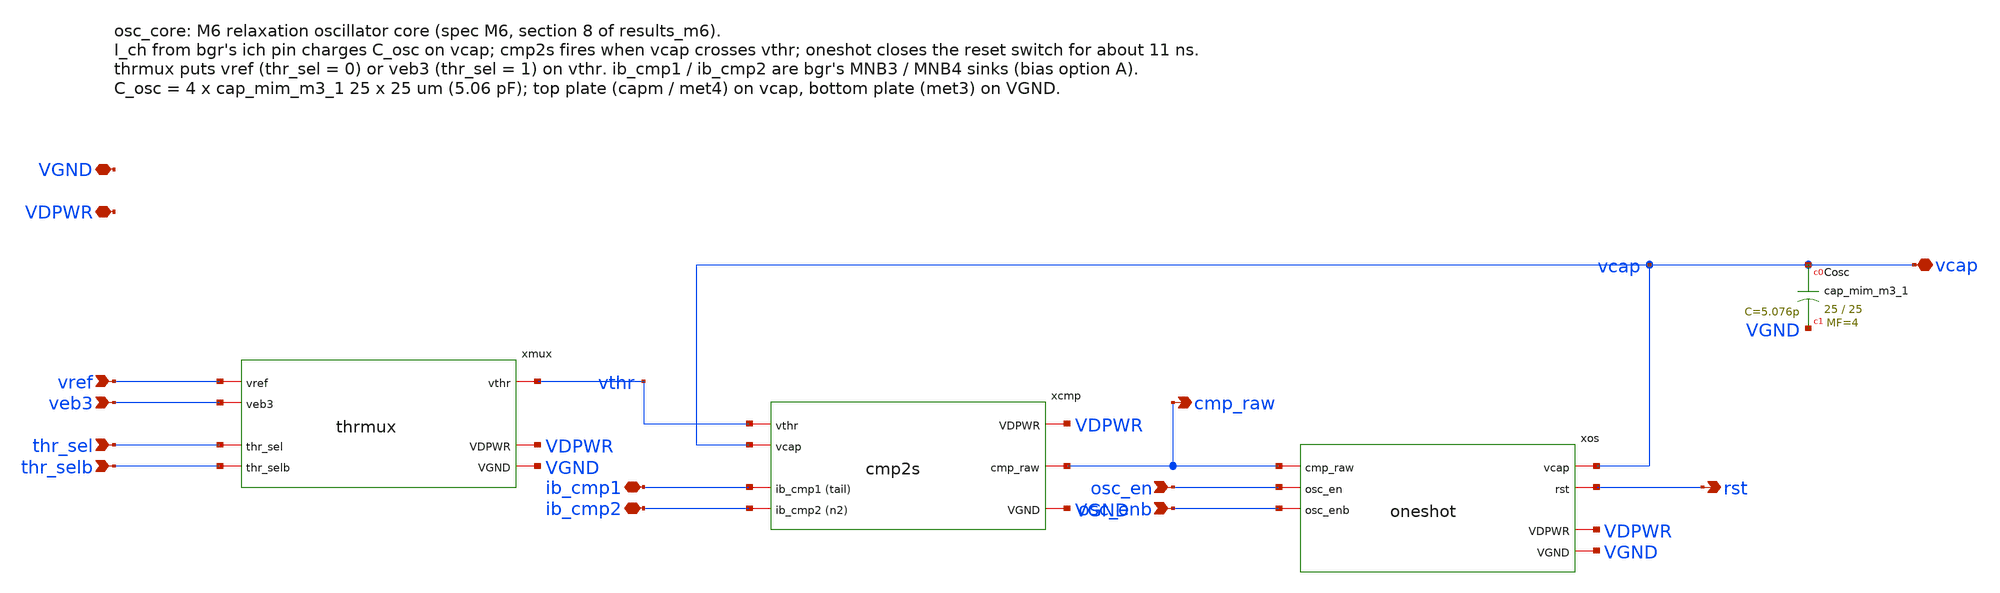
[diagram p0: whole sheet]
** sch_path: xschem/osc_core.sch
**.subckt osc_core vref veb3 thr_sel thr_selb ib_cmp1 ib_cmp2 cmp_raw osc_en osc_enb vcap rst VDPWR
*+ VGND
*.ipin vref
*.ipin veb3
*.ipin thr_sel
*.ipin thr_selb
*.iopin ib_cmp1
*.iopin ib_cmp2
*.opin cmp_raw
*.ipin osc_en
*.ipin osc_enb
*.iopin vcap
*.opin rst
*.iopin VDPWR
*.iopin VGND
xmux vref veb3 thr_sel thr_selb vthr VDPWR VGND thrmux
xcmp vthr vcap ib_cmp1 ib_cmp2 VDPWR cmp_raw VGND cmp2s
xos cmp_raw osc_en osc_enb vcap rst VDPWR VGND oneshot
XCosc vcap VGND sky130_fd_pr__cap_mim_m3_1 W=25 L=25 MF=4 m=4
**.ends

* expanding   symbol:  thrmux.sym # of pins=7
** sym_path: xschem/thrmux.sym
** sch_path: xschem/thrmux.sch
.subckt thrmux vref veb3 thr_sel thr_selb vthr VDPWR VGND
*.ipin thr_sel
*.ipin thr_selb
*.ipin vref
*.ipin veb3
*.iopin vthr
*.iopin VDPWR
*.iopin VGND
xn1 thr_sel seb VGND VGND VDPWR VDPWR sref sky130_fd_sc_hd__nor2_1
xn2 sref thr_selb VGND VGND VDPWR VDPWR seb sky130_fd_sc_hd__nor2_1
xi1 sref VGND VGND VDPWR VDPWR srefb sky130_fd_sc_hd__inv_1
xi2 seb VGND VGND VDPWR VDPWR sebb sky130_fd_sc_hd__inv_1
XMTN1 vref sref vthr VGND sky130_fd_pr__nfet_01v8_lvt L=0.5 W=2 nf=1 ad='int((1 + 1)/2) * 2 / 1 * 0.29'
+ as='int((1 + 2)/2) * 2 / 1 * 0.29' pd='2*int((1 + 1)/2) * (2 / 1 + 0.29)' ps='2*int((1 + 2)/2) * (2 / 1 + 0.29)'
+ nrd='0.29 / 2 ' nrs='0.29 / 2 ' sa=0 sb=0 sd=0 mult=1 m=1
XMTP1 vthr srefb vref VDPWR sky130_fd_pr__pfet_01v8_lvt L=0.5 W=4 nf=1 ad='int((1 + 1)/2) * 4 / 1 * 0.29'
+ as='int((1 + 2)/2) * 4 / 1 * 0.29' pd='2*int((1 + 1)/2) * (4 / 1 + 0.29)' ps='2*int((1 + 2)/2) * (4 / 1 + 0.29)'
+ nrd='0.29 / 4 ' nrs='0.29 / 4 ' sa=0 sb=0 sd=0 mult=1 m=1
XMTN2 vthr seb veb3 VGND sky130_fd_pr__nfet_01v8_lvt L=0.5 W=2 nf=1 ad='int((1 + 1)/2) * 2 / 1 * 0.29'
+ as='int((1 + 2)/2) * 2 / 1 * 0.29' pd='2*int((1 + 1)/2) * (2 / 1 + 0.29)' ps='2*int((1 + 2)/2) * (2 / 1 + 0.29)'
+ nrd='0.29 / 2 ' nrs='0.29 / 2 ' sa=0 sb=0 sd=0 mult=1 m=1
XMTP2 veb3 sebb vthr VDPWR sky130_fd_pr__pfet_01v8_lvt L=0.5 W=4 nf=1 ad='int((1 + 1)/2) * 4 / 1 * 0.29'
+ as='int((1 + 2)/2) * 4 / 1 * 0.29' pd='2*int((1 + 1)/2) * (4 / 1 + 0.29)' ps='2*int((1 + 2)/2) * (4 / 1 + 0.29)'
+ nrd='0.29 / 4 ' nrs='0.29 / 4 ' sa=0 sb=0 sd=0 mult=1 m=1
.ends


* expanding   symbol:  cmp2s.sym # of pins=7
** sym_path: xschem/cmp2s.sym
** sch_path: xschem/cmp2s.sch
.subckt cmp2s vthr vcap ib_cmp1 ib_cmp2 VDPWR cmp_raw VGND
*.iopin VDPWR
*.iopin VGND
*.ipin vthr
*.ipin vcap
*.iopin ib_cmp1
*.iopin ib_cmp2
*.opin cmp_raw
XM2a nd nd VDPWR VDPWR sky130_fd_pr__pfet_01v8_lvt L=4 W=4 nf=1 ad='int((1 + 1)/2) * 4 / 1 * 0.29' as='int((1 + 2)/2) * 4 / 1 * 0.29'
+ pd='2*int((1 + 1)/2) * (4 / 1 + 0.29)' ps='2*int((1 + 2)/2) * (4 / 1 + 0.29)' nrd='0.29 / 4 ' nrs='0.29 / 4 '
+ sa=0 sb=0 sd=0 mult=8 m=8
XM2b n1 nd VDPWR VDPWR sky130_fd_pr__pfet_01v8_lvt L=4 W=4 nf=1 ad='int((1 + 1)/2) * 4 / 1 * 0.29' as='int((1 + 2)/2) * 4 / 1 * 0.29'
+ pd='2*int((1 + 1)/2) * (4 / 1 + 0.29)' ps='2*int((1 + 2)/2) * (4 / 1 + 0.29)' nrd='0.29 / 4 ' nrs='0.29 / 4 '
+ sa=0 sb=0 sd=0 mult=8 m=8
XM1a nd vthr ib_cmp1 VGND sky130_fd_pr__nfet_01v8_lvt L=1.75 W=10 nf=1 ad='int((1 + 1)/2) * 10 / 1 * 0.29'
+ as='int((1 + 2)/2) * 10 / 1 * 0.29' pd='2*int((1 + 1)/2) * (10 / 1 + 0.29)' ps='2*int((1 + 2)/2) * (10 / 1 + 0.29)'
+ nrd='0.29 / 10 ' nrs='0.29 / 10 ' sa=0 sb=0 sd=0 mult=6 m=6
XM1b n1 vcap ib_cmp1 VGND sky130_fd_pr__nfet_01v8_lvt L=1.75 W=10 nf=1 ad='int((1 + 1)/2) * 10 / 1 * 0.29'
+ as='int((1 + 2)/2) * 10 / 1 * 0.29' pd='2*int((1 + 1)/2) * (10 / 1 + 0.29)' ps='2*int((1 + 2)/2) * (10 / 1 + 0.29)'
+ nrd='0.29 / 10 ' nrs='0.29 / 10 ' sa=0 sb=0 sd=0 mult=6 m=6
XM3 ib_cmp2 n1 VDPWR VDPWR sky130_fd_pr__pfet_01v8_lvt L=1 W=4 nf=1 ad='int((1 + 1)/2) * 4 / 1 * 0.29'
+ as='int((1 + 2)/2) * 4 / 1 * 0.29' pd='2*int((1 + 1)/2) * (4 / 1 + 0.29)' ps='2*int((1 + 2)/2) * (4 / 1 + 0.29)'
+ nrd='0.29 / 4 ' nrs='0.29 / 4 ' sa=0 sb=0 sd=0 mult=3 m=3
XMIP x ib_cmp2 VDPWR VDPWR sky130_fd_pr__pfet_01v8 L=1 W=0.42 nf=1 ad='int((1 + 1)/2) * 0.42 / 1 * 0.29'
+ as='int((1 + 2)/2) * 0.42 / 1 * 0.29' pd='2*int((1 + 1)/2) * (0.42 / 1 + 0.29)' ps='2*int((1 + 2)/2) * (0.42 / 1 + 0.29)'
+ nrd='0.29 / 0.42 ' nrs='0.29 / 0.42 ' sa=0 sb=0 sd=0 mult=1 m=1
XMIN x ib_cmp2 VGND VGND sky130_fd_pr__nfet_01v8 L=0.15 W=2 nf=1 ad='int((1 + 1)/2) * 2 / 1 * 0.29' as='int((1 + 2)/2) * 2 / 1 * 0.29'
+ pd='2*int((1 + 1)/2) * (2 / 1 + 0.29)' ps='2*int((1 + 2)/2) * (2 / 1 + 0.29)' nrd='0.29 / 2 ' nrs='0.29 / 2 '
+ sa=0 sb=0 sd=0 mult=1 m=1
xinv x VGND VGND VDPWR VDPWR cmp_raw sky130_fd_sc_hd__inv_1
.ends


* expanding   symbol:  oneshot.sym # of pins=7
** sym_path: xschem/oneshot.sym
** sch_path: xschem/oneshot.sch
.subckt oneshot cmp_raw osc_en osc_enb vcap rst VDPWR VGND
*.ipin cmp_raw
*.ipin osc_enb
*.ipin osc_en
*.iopin vcap
*.opin rst
*.iopin VDPWR
*.iopin VGND
xbck cmp_raw VGND VGND VDPWR VDPWR ck sky130_fd_sc_hd__buf_2
xff ck VDPWR rb VGND VGND VDPWR VDPWR rst sky130_fd_sc_hd__dfrtp_1
xor rst osc_enb VGND VGND VDPWR VDPWR swp sky130_fd_sc_hd__or2_1
xi1 swp VGND VGND VDPWR VDPWR swn sky130_fd_sc_hd__inv_1
xand db osc_en VGND VGND VDPWR VDPWR rb sky130_fd_sc_hd__and2_1
xdl rst db VDPWR VGND dly5
XMDP sw swn VDPWR VDPWR sky130_fd_pr__pfet_01v8 L=0.15 W=2 nf=1 ad='int((1 + 1)/2) * 2 / 1 * 0.29' as='int((1 + 2)/2) * 2 / 1 * 0.29'
+ pd='2*int((1 + 1)/2) * (2 / 1 + 0.29)' ps='2*int((1 + 2)/2) * (2 / 1 + 0.29)' nrd='0.29 / 2 ' nrs='0.29 / 2 '
+ sa=0 sb=0 sd=0 mult=1 m=1
XMDN sw swn VGND VGND sky130_fd_pr__nfet_01v8 L=1.5 W=0.42 nf=1 ad='int((1 + 1)/2) * 0.42 / 1 * 0.29'
+ as='int((1 + 2)/2) * 0.42 / 1 * 0.29' pd='2*int((1 + 1)/2) * (0.42 / 1 + 0.29)' ps='2*int((1 + 2)/2) * (0.42 / 1 + 0.29)'
+ nrd='0.29 / 0.42 ' nrs='0.29 / 0.42 ' sa=0 sb=0 sd=0 mult=1 m=1
XMRST vcap sw VGND VGND sky130_fd_pr__nfet_01v8 L=0.5 W=6 nf=1 ad='int((1 + 1)/2) * 6 / 1 * 0.29' as='int((1 + 2)/2) * 6 / 1 * 0.29'
+ pd='2*int((1 + 1)/2) * (6 / 1 + 0.29)' ps='2*int((1 + 2)/2) * (6 / 1 + 0.29)' nrd='0.29 / 6 ' nrs='0.29 / 6 '
+ sa=0 sb=0 sd=0 mult=2 m=2
.ends


* expanding   symbol:  dly5.sym # of pins=4
** sym_path: xschem/dly5.sym
** sch_path: xschem/dly5.sch
.subckt dly5 a y VDPWR VGND
*.iopin VDPWR
*.iopin VGND
*.ipin a
*.opin y
XMP1 d1 a VDPWR VDPWR sky130_fd_pr__pfet_01v8 L=2.3 W=1 nf=1 ad='int((1 + 1)/2) * 1 / 1 * 0.29' as='int((1 + 2)/2) * 1 / 1 * 0.29'
+ pd='2*int((1 + 1)/2) * (1 / 1 + 0.29)' ps='2*int((1 + 2)/2) * (1 / 1 + 0.29)' nrd='0.29 / 1 ' nrs='0.29 / 1 '
+ sa=0 sb=0 sd=0 mult=1 m=1
XMN1 d1 a VGND VGND sky130_fd_pr__nfet_01v8 L=2.3 W=0.42 nf=1 ad='int((1 + 1)/2) * 0.42 / 1 * 0.29' as='int((1 + 2)/2) * 0.42 / 1 * 0.29'
+ pd='2*int((1 + 1)/2) * (0.42 / 1 + 0.29)' ps='2*int((1 + 2)/2) * (0.42 / 1 + 0.29)' nrd='0.29 / 0.42 '
+ nrs='0.29 / 0.42 ' sa=0 sb=0 sd=0 mult=1 m=1
XMP2 d2 d1 VDPWR VDPWR sky130_fd_pr__pfet_01v8 L=2.3 W=1 nf=1 ad='int((1 + 1)/2) * 1 / 1 * 0.29' as='int((1 + 2)/2) * 1 / 1 * 0.29'
+ pd='2*int((1 + 1)/2) * (1 / 1 + 0.29)' ps='2*int((1 + 2)/2) * (1 / 1 + 0.29)' nrd='0.29 / 1 ' nrs='0.29 / 1 '
+ sa=0 sb=0 sd=0 mult=1 m=1
XMN2 d2 d1 VGND VGND sky130_fd_pr__nfet_01v8 L=2.3 W=0.42 nf=1 ad='int((1 + 1)/2) * 0.42 / 1 * 0.29'
+ as='int((1 + 2)/2) * 0.42 / 1 * 0.29' pd='2*int((1 + 1)/2) * (0.42 / 1 + 0.29)' ps='2*int((1 + 2)/2) * (0.42 / 1 + 0.29)'
+ nrd='0.29 / 0.42 ' nrs='0.29 / 0.42 ' sa=0 sb=0 sd=0 mult=1 m=1
XMP3 d3 d2 VDPWR VDPWR sky130_fd_pr__pfet_01v8 L=2.3 W=1 nf=1 ad='int((1 + 1)/2) * 1 / 1 * 0.29' as='int((1 + 2)/2) * 1 / 1 * 0.29'
+ pd='2*int((1 + 1)/2) * (1 / 1 + 0.29)' ps='2*int((1 + 2)/2) * (1 / 1 + 0.29)' nrd='0.29 / 1 ' nrs='0.29 / 1 '
+ sa=0 sb=0 sd=0 mult=1 m=1
XMN3 d3 d2 VGND VGND sky130_fd_pr__nfet_01v8 L=2.3 W=0.42 nf=1 ad='int((1 + 1)/2) * 0.42 / 1 * 0.29'
+ as='int((1 + 2)/2) * 0.42 / 1 * 0.29' pd='2*int((1 + 1)/2) * (0.42 / 1 + 0.29)' ps='2*int((1 + 2)/2) * (0.42 / 1 + 0.29)'
+ nrd='0.29 / 0.42 ' nrs='0.29 / 0.42 ' sa=0 sb=0 sd=0 mult=1 m=1
XMP4 d4 d3 VDPWR VDPWR sky130_fd_pr__pfet_01v8 L=2.3 W=1 nf=1 ad='int((1 + 1)/2) * 1 / 1 * 0.29' as='int((1 + 2)/2) * 1 / 1 * 0.29'
+ pd='2*int((1 + 1)/2) * (1 / 1 + 0.29)' ps='2*int((1 + 2)/2) * (1 / 1 + 0.29)' nrd='0.29 / 1 ' nrs='0.29 / 1 '
+ sa=0 sb=0 sd=0 mult=1 m=1
XMN4 d4 d3 VGND VGND sky130_fd_pr__nfet_01v8 L=2.3 W=0.42 nf=1 ad='int((1 + 1)/2) * 0.42 / 1 * 0.29'
+ as='int((1 + 2)/2) * 0.42 / 1 * 0.29' pd='2*int((1 + 1)/2) * (0.42 / 1 + 0.29)' ps='2*int((1 + 2)/2) * (0.42 / 1 + 0.29)'
+ nrd='0.29 / 0.42 ' nrs='0.29 / 0.42 ' sa=0 sb=0 sd=0 mult=1 m=1
XMP5 y d4 VDPWR VDPWR sky130_fd_pr__pfet_01v8 L=2.3 W=1 nf=1 ad='int((1 + 1)/2) * 1 / 1 * 0.29' as='int((1 + 2)/2) * 1 / 1 * 0.29'
+ pd='2*int((1 + 1)/2) * (1 / 1 + 0.29)' ps='2*int((1 + 2)/2) * (1 / 1 + 0.29)' nrd='0.29 / 1 ' nrs='0.29 / 1 '
+ sa=0 sb=0 sd=0 mult=1 m=1
XMN5 y d4 VGND VGND sky130_fd_pr__nfet_01v8 L=2.3 W=0.42 nf=1 ad='int((1 + 1)/2) * 0.42 / 1 * 0.29' as='int((1 + 2)/2) * 0.42 / 1 * 0.29'
+ pd='2*int((1 + 1)/2) * (0.42 / 1 + 0.29)' ps='2*int((1 + 2)/2) * (0.42 / 1 + 0.29)' nrd='0.29 / 0.42 '
+ nrs='0.29 / 0.42 ' sa=0 sb=0 sd=0 mult=1 m=1
.ends

.end
